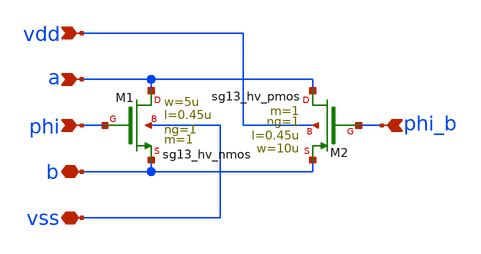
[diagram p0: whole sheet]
** sch_path: 3_real_circuits/tg_hv.sch
**.subckt tg_hv phi_b phi a vdd vss b
*.ipin phi_b
*.ipin phi
*.ipin a
*.ipin vdd
*.iopin vss
*.iopin b
XM2 a phi_b b vdd sg13_hv_pmos w=10u l=0.45u ng=1 m=1 mm_ok=1
XM1 a phi b vss sg13_hv_nmos w=5u l=0.45u ng=1 m=1 mm_ok=1
**.ends
.end
